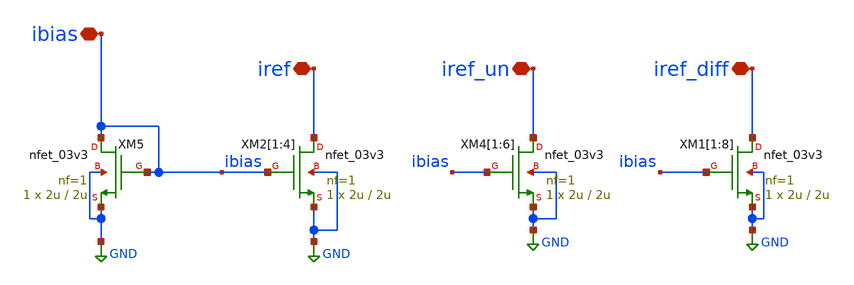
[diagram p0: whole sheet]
** sch_path: Voltage_Reference/LDO/CM_block.sch
**.subckt CM_block ibias iref iref_un iref_diff
*.iopin ibias
*.iopin iref
*.iopin iref_un
*.iopin iref_diff
XM4[1] iref_un ibias GND GND nfet_03v3 L=2u W=2u nf=1 ad='int((nf+1)/2) * W/nf * 0.18u' as='int((nf+2)/2) * W/nf * 0.18u'
+ pd='2*int((nf+1)/2) * (W/nf + 0.18u)' ps='2*int((nf+2)/2) * (W/nf + 0.18u)' nrd='0.18u / W' nrs='0.18u / W'
+ sa=0 sb=0 sd=0 m=1
XM4[2] iref_un ibias GND GND nfet_03v3 L=2u W=2u nf=1 ad='int((nf+1)/2) * W/nf * 0.18u' as='int((nf+2)/2) * W/nf * 0.18u'
+ pd='2*int((nf+1)/2) * (W/nf + 0.18u)' ps='2*int((nf+2)/2) * (W/nf + 0.18u)' nrd='0.18u / W' nrs='0.18u / W'
+ sa=0 sb=0 sd=0 m=1
XM4[3] iref_un ibias GND GND nfet_03v3 L=2u W=2u nf=1 ad='int((nf+1)/2) * W/nf * 0.18u' as='int((nf+2)/2) * W/nf * 0.18u'
+ pd='2*int((nf+1)/2) * (W/nf + 0.18u)' ps='2*int((nf+2)/2) * (W/nf + 0.18u)' nrd='0.18u / W' nrs='0.18u / W'
+ sa=0 sb=0 sd=0 m=1
XM4[4] iref_un ibias GND GND nfet_03v3 L=2u W=2u nf=1 ad='int((nf+1)/2) * W/nf * 0.18u' as='int((nf+2)/2) * W/nf * 0.18u'
+ pd='2*int((nf+1)/2) * (W/nf + 0.18u)' ps='2*int((nf+2)/2) * (W/nf + 0.18u)' nrd='0.18u / W' nrs='0.18u / W'
+ sa=0 sb=0 sd=0 m=1
XM4[5] iref_un ibias GND GND nfet_03v3 L=2u W=2u nf=1 ad='int((nf+1)/2) * W/nf * 0.18u' as='int((nf+2)/2) * W/nf * 0.18u'
+ pd='2*int((nf+1)/2) * (W/nf + 0.18u)' ps='2*int((nf+2)/2) * (W/nf + 0.18u)' nrd='0.18u / W' nrs='0.18u / W'
+ sa=0 sb=0 sd=0 m=1
XM4[6] iref_un ibias GND GND nfet_03v3 L=2u W=2u nf=1 ad='int((nf+1)/2) * W/nf * 0.18u' as='int((nf+2)/2) * W/nf * 0.18u'
+ pd='2*int((nf+1)/2) * (W/nf + 0.18u)' ps='2*int((nf+2)/2) * (W/nf + 0.18u)' nrd='0.18u / W' nrs='0.18u / W'
+ sa=0 sb=0 sd=0 m=1
XM1[1] iref_diff ibias GND GND nfet_03v3 L=2u W=2u nf=1 ad='int((nf+1)/2) * W/nf * 0.18u' as='int((nf+2)/2) * W/nf * 0.18u'
+ pd='2*int((nf+1)/2) * (W/nf + 0.18u)' ps='2*int((nf+2)/2) * (W/nf + 0.18u)' nrd='0.18u / W' nrs='0.18u / W'
+ sa=0 sb=0 sd=0 m=1
XM1[2] iref_diff ibias GND GND nfet_03v3 L=2u W=2u nf=1 ad='int((nf+1)/2) * W/nf * 0.18u' as='int((nf+2)/2) * W/nf * 0.18u'
+ pd='2*int((nf+1)/2) * (W/nf + 0.18u)' ps='2*int((nf+2)/2) * (W/nf + 0.18u)' nrd='0.18u / W' nrs='0.18u / W'
+ sa=0 sb=0 sd=0 m=1
XM1[3] iref_diff ibias GND GND nfet_03v3 L=2u W=2u nf=1 ad='int((nf+1)/2) * W/nf * 0.18u' as='int((nf+2)/2) * W/nf * 0.18u'
+ pd='2*int((nf+1)/2) * (W/nf + 0.18u)' ps='2*int((nf+2)/2) * (W/nf + 0.18u)' nrd='0.18u / W' nrs='0.18u / W'
+ sa=0 sb=0 sd=0 m=1
XM1[4] iref_diff ibias GND GND nfet_03v3 L=2u W=2u nf=1 ad='int((nf+1)/2) * W/nf * 0.18u' as='int((nf+2)/2) * W/nf * 0.18u'
+ pd='2*int((nf+1)/2) * (W/nf + 0.18u)' ps='2*int((nf+2)/2) * (W/nf + 0.18u)' nrd='0.18u / W' nrs='0.18u / W'
+ sa=0 sb=0 sd=0 m=1
XM1[5] iref_diff ibias GND GND nfet_03v3 L=2u W=2u nf=1 ad='int((nf+1)/2) * W/nf * 0.18u' as='int((nf+2)/2) * W/nf * 0.18u'
+ pd='2*int((nf+1)/2) * (W/nf + 0.18u)' ps='2*int((nf+2)/2) * (W/nf + 0.18u)' nrd='0.18u / W' nrs='0.18u / W'
+ sa=0 sb=0 sd=0 m=1
XM1[6] iref_diff ibias GND GND nfet_03v3 L=2u W=2u nf=1 ad='int((nf+1)/2) * W/nf * 0.18u' as='int((nf+2)/2) * W/nf * 0.18u'
+ pd='2*int((nf+1)/2) * (W/nf + 0.18u)' ps='2*int((nf+2)/2) * (W/nf + 0.18u)' nrd='0.18u / W' nrs='0.18u / W'
+ sa=0 sb=0 sd=0 m=1
XM1[7] iref_diff ibias GND GND nfet_03v3 L=2u W=2u nf=1 ad='int((nf+1)/2) * W/nf * 0.18u' as='int((nf+2)/2) * W/nf * 0.18u'
+ pd='2*int((nf+1)/2) * (W/nf + 0.18u)' ps='2*int((nf+2)/2) * (W/nf + 0.18u)' nrd='0.18u / W' nrs='0.18u / W'
+ sa=0 sb=0 sd=0 m=1
XM1[8] iref_diff ibias GND GND nfet_03v3 L=2u W=2u nf=1 ad='int((nf+1)/2) * W/nf * 0.18u' as='int((nf+2)/2) * W/nf * 0.18u'
+ pd='2*int((nf+1)/2) * (W/nf + 0.18u)' ps='2*int((nf+2)/2) * (W/nf + 0.18u)' nrd='0.18u / W' nrs='0.18u / W'
+ sa=0 sb=0 sd=0 m=1
XM2[1] iref ibias GND GND nfet_03v3 L=2u W=2u nf=1 ad='int((nf+1)/2) * W/nf * 0.18u' as='int((nf+2)/2) * W/nf * 0.18u'
+ pd='2*int((nf+1)/2) * (W/nf + 0.18u)' ps='2*int((nf+2)/2) * (W/nf + 0.18u)' nrd='0.18u / W' nrs='0.18u / W'
+ sa=0 sb=0 sd=0 m=1
XM2[2] iref ibias GND GND nfet_03v3 L=2u W=2u nf=1 ad='int((nf+1)/2) * W/nf * 0.18u' as='int((nf+2)/2) * W/nf * 0.18u'
+ pd='2*int((nf+1)/2) * (W/nf + 0.18u)' ps='2*int((nf+2)/2) * (W/nf + 0.18u)' nrd='0.18u / W' nrs='0.18u / W'
+ sa=0 sb=0 sd=0 m=1
XM2[3] iref ibias GND GND nfet_03v3 L=2u W=2u nf=1 ad='int((nf+1)/2) * W/nf * 0.18u' as='int((nf+2)/2) * W/nf * 0.18u'
+ pd='2*int((nf+1)/2) * (W/nf + 0.18u)' ps='2*int((nf+2)/2) * (W/nf + 0.18u)' nrd='0.18u / W' nrs='0.18u / W'
+ sa=0 sb=0 sd=0 m=1
XM2[4] iref ibias GND GND nfet_03v3 L=2u W=2u nf=1 ad='int((nf+1)/2) * W/nf * 0.18u' as='int((nf+2)/2) * W/nf * 0.18u'
+ pd='2*int((nf+1)/2) * (W/nf + 0.18u)' ps='2*int((nf+2)/2) * (W/nf + 0.18u)' nrd='0.18u / W' nrs='0.18u / W'
+ sa=0 sb=0 sd=0 m=1
XM5 ibias ibias GND GND nfet_03v3 L=2u W=2u nf=1 ad='int((nf+1)/2) * W/nf * 0.18u' as='int((nf+2)/2) * W/nf * 0.18u'
+ pd='2*int((nf+1)/2) * (W/nf + 0.18u)' ps='2*int((nf+2)/2) * (W/nf + 0.18u)' nrd='0.18u / W' nrs='0.18u / W'
+ sa=0 sb=0 sd=0 m=1
**.ends
.GLOBAL GND
.end
